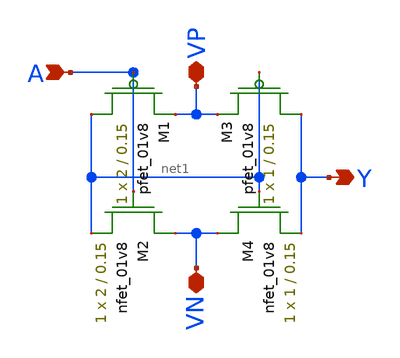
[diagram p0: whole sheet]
** sch_path: DRAM_Components/Schematic/ADC1bit.sch
**.subckt ADC1bit A Y VP VN
*.ipin A
*.opin Y
*.iopin VP
*.iopin VN
XM1 net1 A VP VDD sky130_fd_pr__pfet_01v8 L=0.15 W=2 nf=1 ad='int((nf+1)/2) * W/nf * 0.29' as='int((nf+2)/2) * W/nf * 0.29'
+ pd='2*int((nf+1)/2) * (W/nf + 0.29)' ps='2*int((nf+2)/2) * (W/nf + 0.29)' nrd='0.29 / W' nrs='0.29 / W'
+ sa=0 sb=0 sd=0 mult=1 m=1
XM2 VN A net1 GND sky130_fd_pr__nfet_01v8 L=0.15 W=2 nf=1 ad='int((nf+1)/2) * W/nf * 0.29' as='int((nf+2)/2) * W/nf * 0.29'
+ pd='2*int((nf+1)/2) * (W/nf + 0.29)' ps='2*int((nf+2)/2) * (W/nf + 0.29)' nrd='0.29 / W' nrs='0.29 / W'
+ sa=0 sb=0 sd=0 mult=1 m=1
XM3 Y net1 VP VDD sky130_fd_pr__pfet_01v8 L=0.15 W=1 nf=1 ad='int((nf+1)/2) * W/nf * 0.29' as='int((nf+2)/2) * W/nf * 0.29'
+ pd='2*int((nf+1)/2) * (W/nf + 0.29)' ps='2*int((nf+2)/2) * (W/nf + 0.29)' nrd='0.29 / W' nrs='0.29 / W'
+ sa=0 sb=0 sd=0 mult=1 m=1
XM4 VN net1 Y GND sky130_fd_pr__nfet_01v8 L=0.15 W=1 nf=1 ad='int((nf+1)/2) * W/nf * 0.29' as='int((nf+2)/2) * W/nf * 0.29'
+ pd='2*int((nf+1)/2) * (W/nf + 0.29)' ps='2*int((nf+2)/2) * (W/nf + 0.29)' nrd='0.29 / W' nrs='0.29 / W'
+ sa=0 sb=0 sd=0 mult=1 m=1
**.ends
.end
